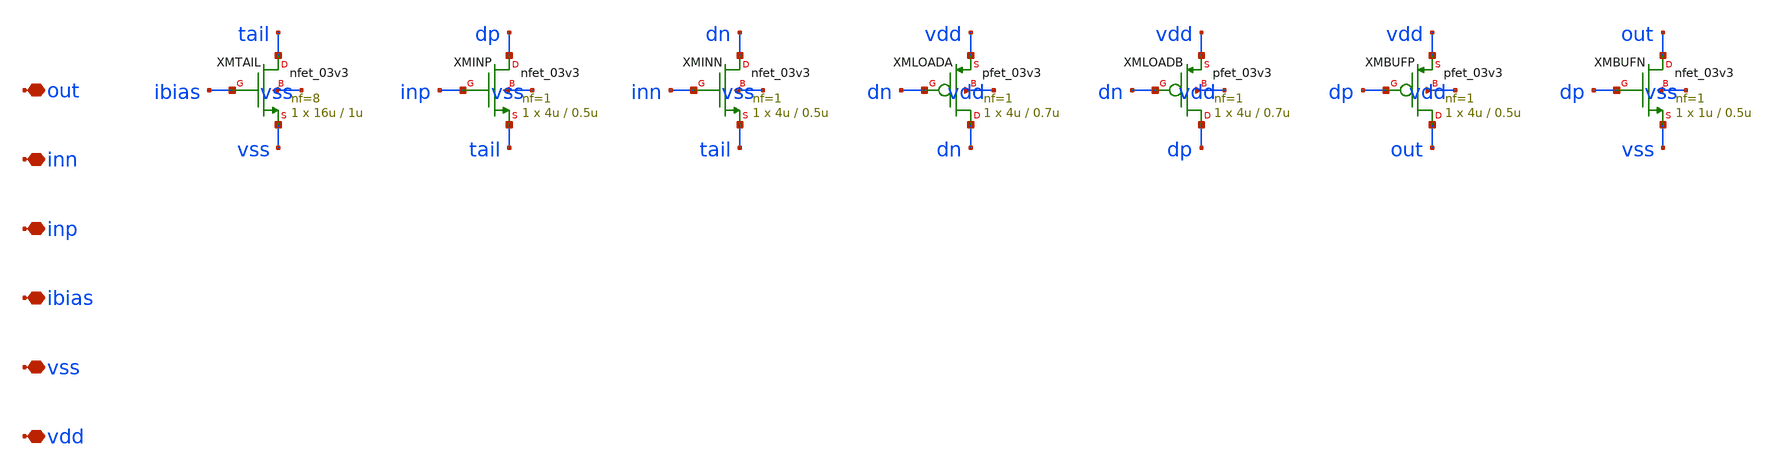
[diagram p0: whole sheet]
** sch_path: design/rcosc_comparator.sch
**.subckt rcosc_comparator vdd vss ibias inp inn out
*.iopin vdd
*.iopin vss
*.iopin ibias
*.iopin inp
*.iopin inn
*.iopin out
XMTAIL tail ibias vss vss nfet_03v3 L=1u W=16u nf=8 ad='int((nf+1)/2) * W/nf * 0.18u' as='int((nf+2)/2) * W/nf * 0.18u'
+ pd='2*int((nf+1)/2) * (W/nf + 0.18u)' ps='2*int((nf+2)/2) * (W/nf + 0.18u)' nrd='0.18u / W' nrs='0.18u / W'
+ sa=0 sb=0 sd=0 m=1
XMINP dp inp tail vss nfet_03v3 L=0.5u W=4u nf=1 ad='int((nf+1)/2) * W/nf * 0.18u' as='int((nf+2)/2) * W/nf * 0.18u'
+ pd='2*int((nf+1)/2) * (W/nf + 0.18u)' ps='2*int((nf+2)/2) * (W/nf + 0.18u)' nrd='0.18u / W' nrs='0.18u / W'
+ sa=0 sb=0 sd=0 m=1
XMINN dn inn tail vss nfet_03v3 L=0.5u W=4u nf=1 ad='int((nf+1)/2) * W/nf * 0.18u' as='int((nf+2)/2) * W/nf * 0.18u'
+ pd='2*int((nf+1)/2) * (W/nf + 0.18u)' ps='2*int((nf+2)/2) * (W/nf + 0.18u)' nrd='0.18u / W' nrs='0.18u / W'
+ sa=0 sb=0 sd=0 m=1
XMLOADA dn dn vdd vdd pfet_03v3 L=0.7u W=4u nf=1 ad='int((nf+1)/2) * W/nf * 0.18u' as='int((nf+2)/2) * W/nf * 0.18u'
+ pd='2*int((nf+1)/2) * (W/nf + 0.18u)' ps='2*int((nf+2)/2) * (W/nf + 0.18u)' nrd='0.18u / W' nrs='0.18u / W'
+ sa=0 sb=0 sd=0 m=1
XMLOADB dp dn vdd vdd pfet_03v3 L=0.7u W=4u nf=1 ad='int((nf+1)/2) * W/nf * 0.18u' as='int((nf+2)/2) * W/nf * 0.18u'
+ pd='2*int((nf+1)/2) * (W/nf + 0.18u)' ps='2*int((nf+2)/2) * (W/nf + 0.18u)' nrd='0.18u / W' nrs='0.18u / W'
+ sa=0 sb=0 sd=0 m=1
XMBUFP out dp vdd vdd pfet_03v3 L=0.5u W=4u nf=1 ad='int((nf+1)/2) * W/nf * 0.18u' as='int((nf+2)/2) * W/nf * 0.18u'
+ pd='2*int((nf+1)/2) * (W/nf + 0.18u)' ps='2*int((nf+2)/2) * (W/nf + 0.18u)' nrd='0.18u / W' nrs='0.18u / W'
+ sa=0 sb=0 sd=0 m=1
XMBUFN out dp vss vss nfet_03v3 L=0.5u W=1u nf=1 ad='int((nf+1)/2) * W/nf * 0.18u' as='int((nf+2)/2) * W/nf * 0.18u'
+ pd='2*int((nf+1)/2) * (W/nf + 0.18u)' ps='2*int((nf+2)/2) * (W/nf + 0.18u)' nrd='0.18u / W' nrs='0.18u / W'
+ sa=0 sb=0 sd=0 m=1
**.ends
.end
